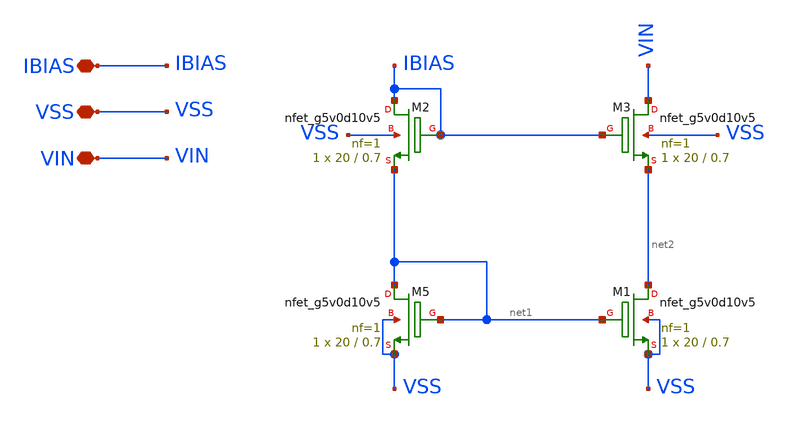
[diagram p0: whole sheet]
** sch_path: old stuff/amplifiers/current_mirrors/cascode_current_mirror/current_mirror.sch
**.subckt current_mirror IBIAS VSS VIN
*.iopin IBIAS
*.iopin VSS
*.iopin VIN
XM5 net1 net1 VSS VSS sky130_fd_pr__nfet_g5v0d10v5 L=0.7 W=20 nf=1 ad='int((1 + 1)/2) * 20 / 1 * 0.29'
+ as='int((1 + 2)/2) * 20 / 1 * 0.29' pd='2*int((1 + 1)/2) * (20 / 1 + 0.29)' ps='2*int((1 + 2)/2) * (20 / 1 + 0.29)'
+ nrd='0.29 / 20 ' nrs='0.29 / 20 ' sa=0 sb=0 sd=0 mult=1 m=1
XM1 net2 net1 VSS VSS sky130_fd_pr__nfet_g5v0d10v5 L=0.7 W=20 nf=1 ad='int((1 + 1)/2) * 20 / 1 * 0.29'
+ as='int((1 + 2)/2) * 20 / 1 * 0.29' pd='2*int((1 + 1)/2) * (20 / 1 + 0.29)' ps='2*int((1 + 2)/2) * (20 / 1 + 0.29)'
+ nrd='0.29 / 20 ' nrs='0.29 / 20 ' sa=0 sb=0 sd=0 mult=1 m=1
XM2 IBIAS IBIAS net1 VSS sky130_fd_pr__nfet_g5v0d10v5 L=0.7 W=20 nf=1 ad='int((1 + 1)/2) * 20 / 1 * 0.29'
+ as='int((1 + 2)/2) * 20 / 1 * 0.29' pd='2*int((1 + 1)/2) * (20 / 1 + 0.29)' ps='2*int((1 + 2)/2) * (20 / 1 + 0.29)'
+ nrd='0.29 / 20 ' nrs='0.29 / 20 ' sa=0 sb=0 sd=0 mult=1 m=1
XM3 VIN IBIAS net2 VSS sky130_fd_pr__nfet_g5v0d10v5 L=0.7 W=20 nf=1 ad='int((1 + 1)/2) * 20 / 1 * 0.29'
+ as='int((1 + 2)/2) * 20 / 1 * 0.29' pd='2*int((1 + 1)/2) * (20 / 1 + 0.29)' ps='2*int((1 + 2)/2) * (20 / 1 + 0.29)'
+ nrd='0.29 / 20 ' nrs='0.29 / 20 ' sa=0 sb=0 sd=0 mult=1 m=1
**.ends
.end
